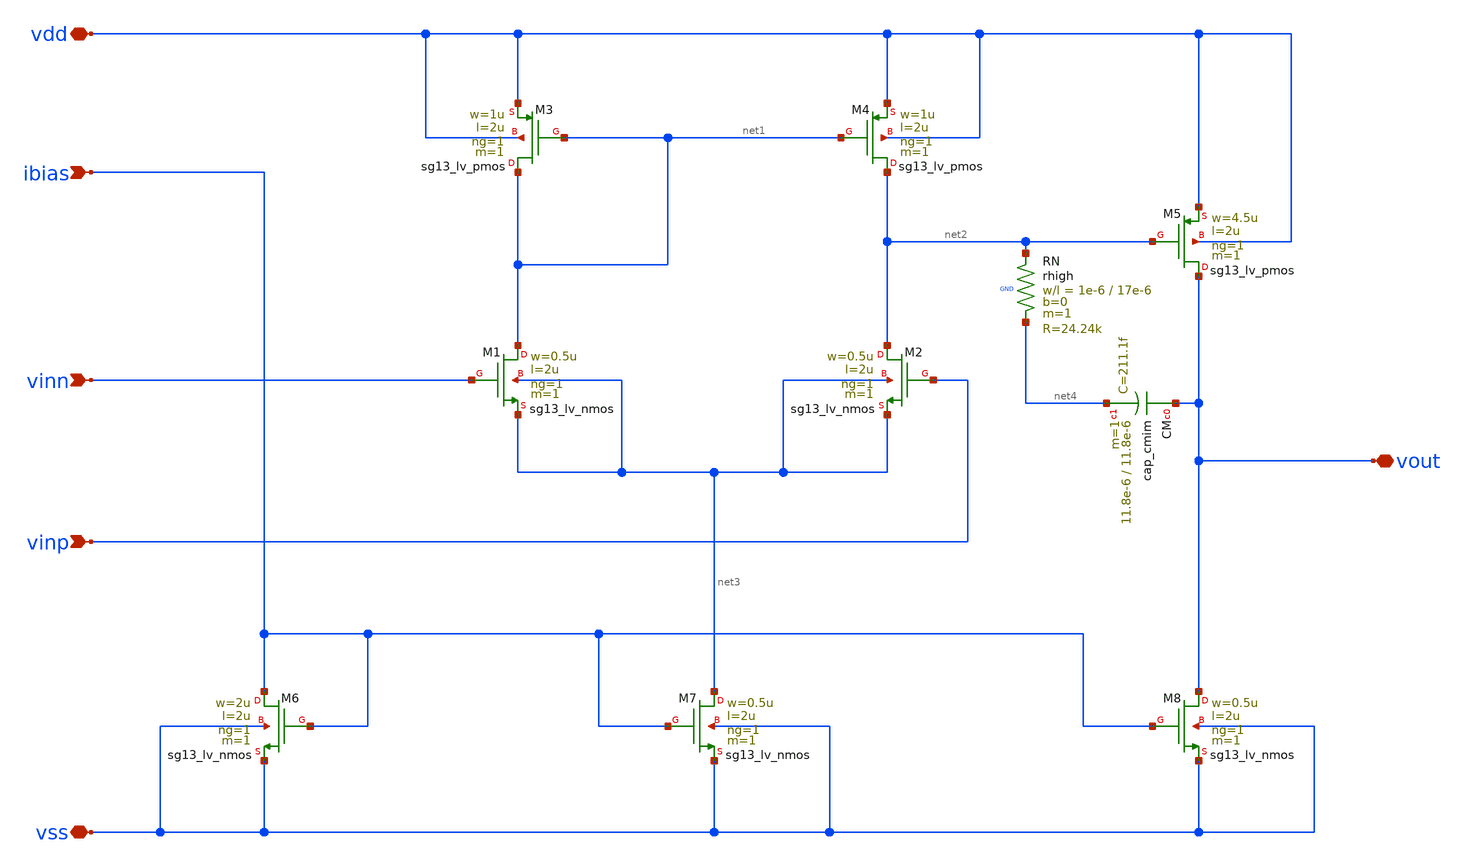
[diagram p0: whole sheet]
** sch_path: Testbench/ota-2stage.sch
**.subckt ota-2stage vdd vss ibias vout vinn vinp
*.iopin vdd
*.iopin vss
*.ipin ibias
*.iopin vout
*.ipin vinn
*.ipin vinp
XM1 net1 vinn net3 net3 sg13_lv_nmos w=0.5u l=2u ng=1 m=1 mm_ok=1
XM2 net2 vinp net3 net3 sg13_lv_nmos w=0.5u l=2u ng=1 m=1 mm_ok=1
XM4 net2 net1 vdd vdd sg13_lv_pmos w=1u l=2u ng=1 m=1 mm_ok=1
XM3 net1 net1 vdd vdd sg13_lv_pmos w=1u l=2u ng=1 m=1 mm_ok=1
XM5 vout net2 vdd vdd sg13_lv_pmos w=4.5u l=2u ng=1 m=1 mm_ok=1
XM6 ibias ibias vss vss sg13_lv_nmos w=2u l=2u ng=1 m=1 mm_ok=1
XM7 net3 ibias vss vss sg13_lv_nmos w=0.5u l=2u ng=1 m=1 mm_ok=1
XM8 vout ibias vss vss sg13_lv_nmos w=0.5u l=2u ng=1 m=1 mm_ok=1
XCM vout net4 cap_cmim w=11.8e-6 l=11.8e-6 m=1 mm_ok=1
XRN net2 net4 GND rhigh w=1e-6 l=17e-6 m=1 b=0 mm_ok=1
**.ends
.end
